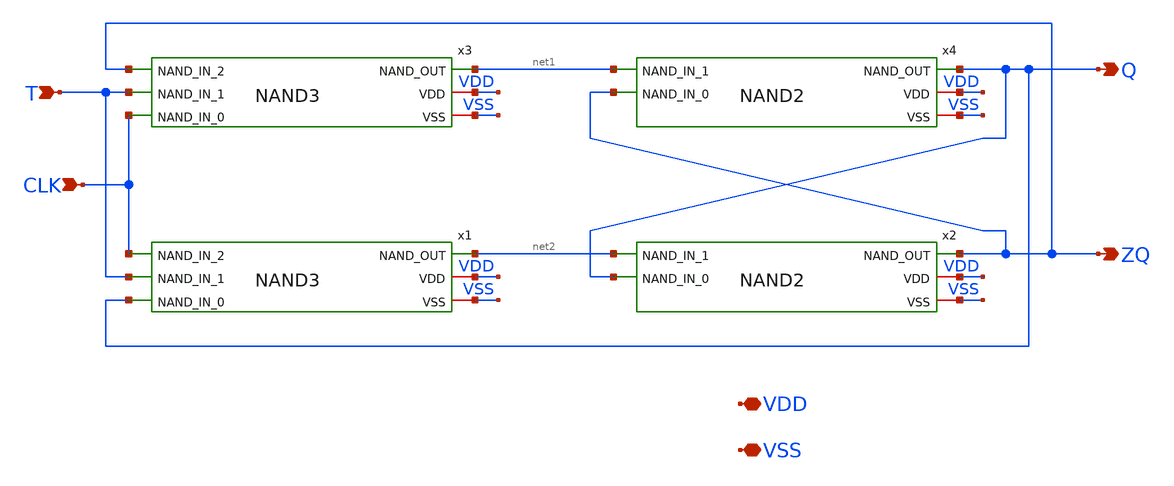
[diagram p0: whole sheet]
** sch_path: xschem/untitled-3.sch
**.subckt untitled-3 VDD VSS CLK T ZQ Q
*.iopin VDD
*.iopin VSS
*.ipin CLK
*.ipin T
*.opin ZQ
*.opin Q
x1 net2 CLK VDD T VSS Q NAND3
x2 ZQ VDD net2 VSS Q NAND2
x3 net1 ZQ VDD T VSS CLK NAND3
x4 Q VDD net1 VSS ZQ NAND2
**.ends
.end
